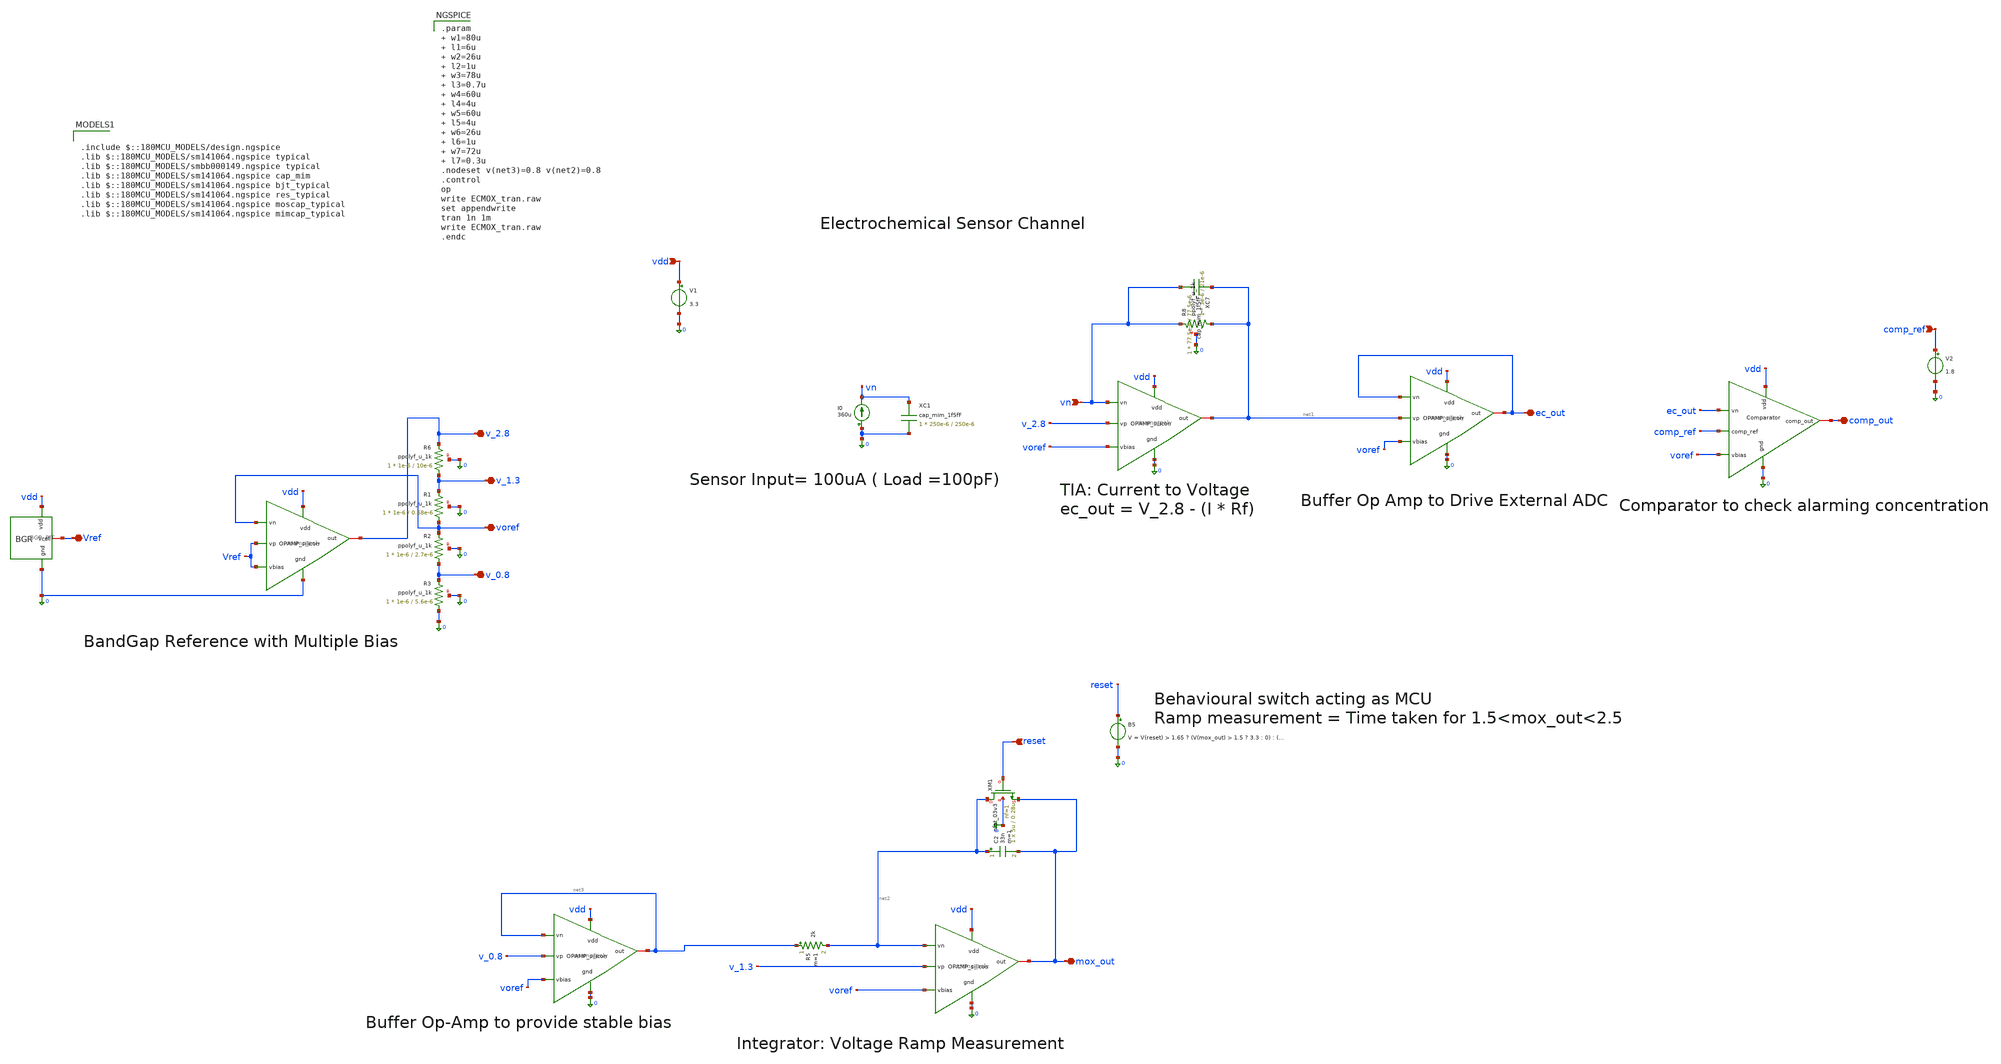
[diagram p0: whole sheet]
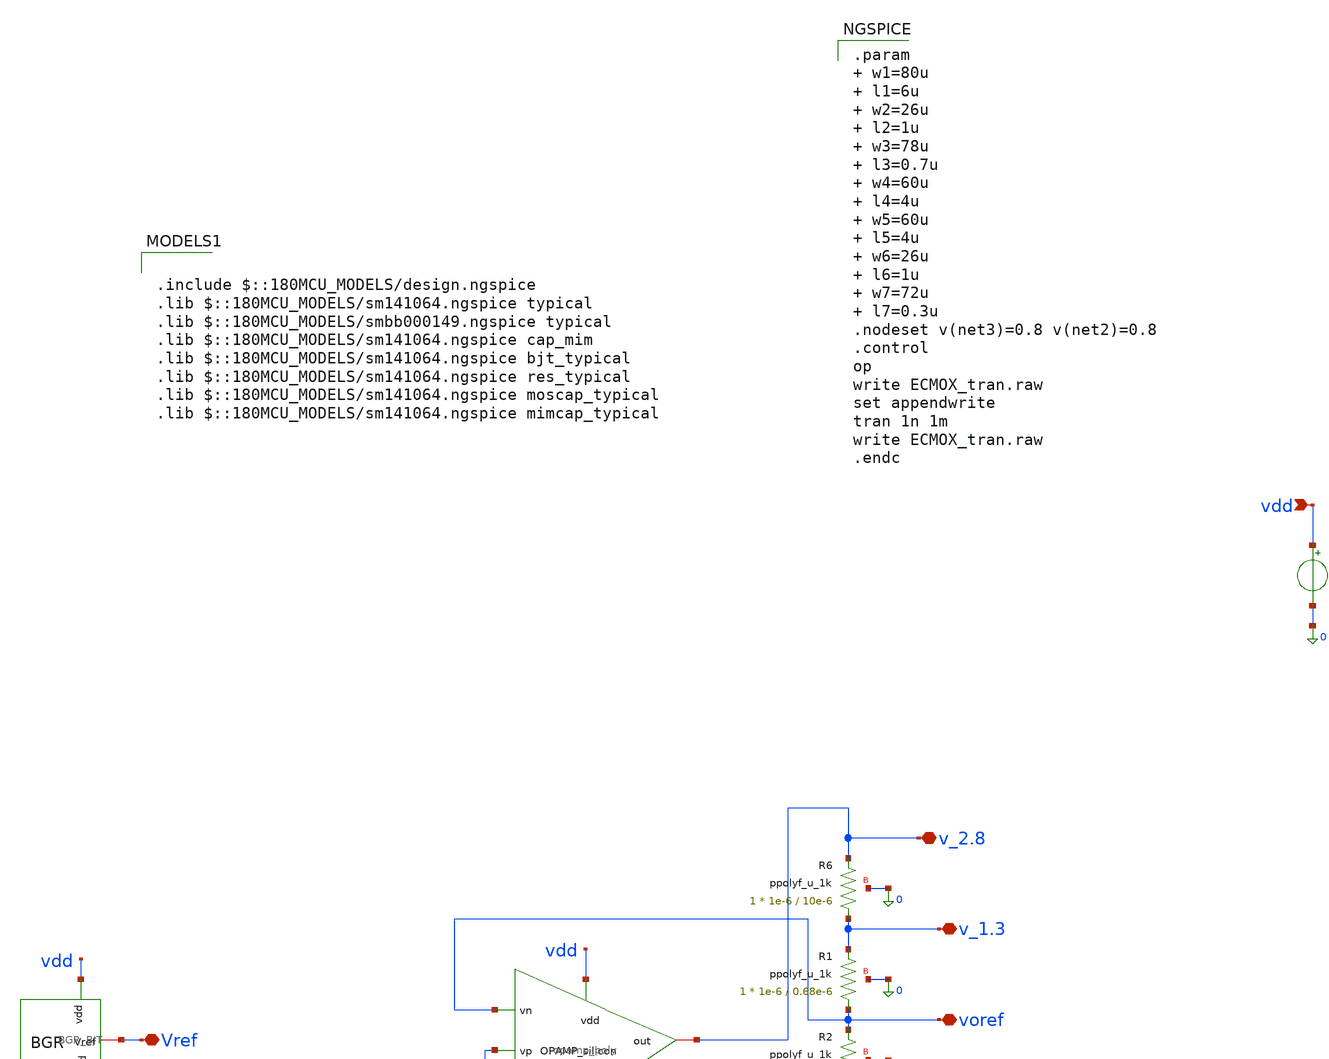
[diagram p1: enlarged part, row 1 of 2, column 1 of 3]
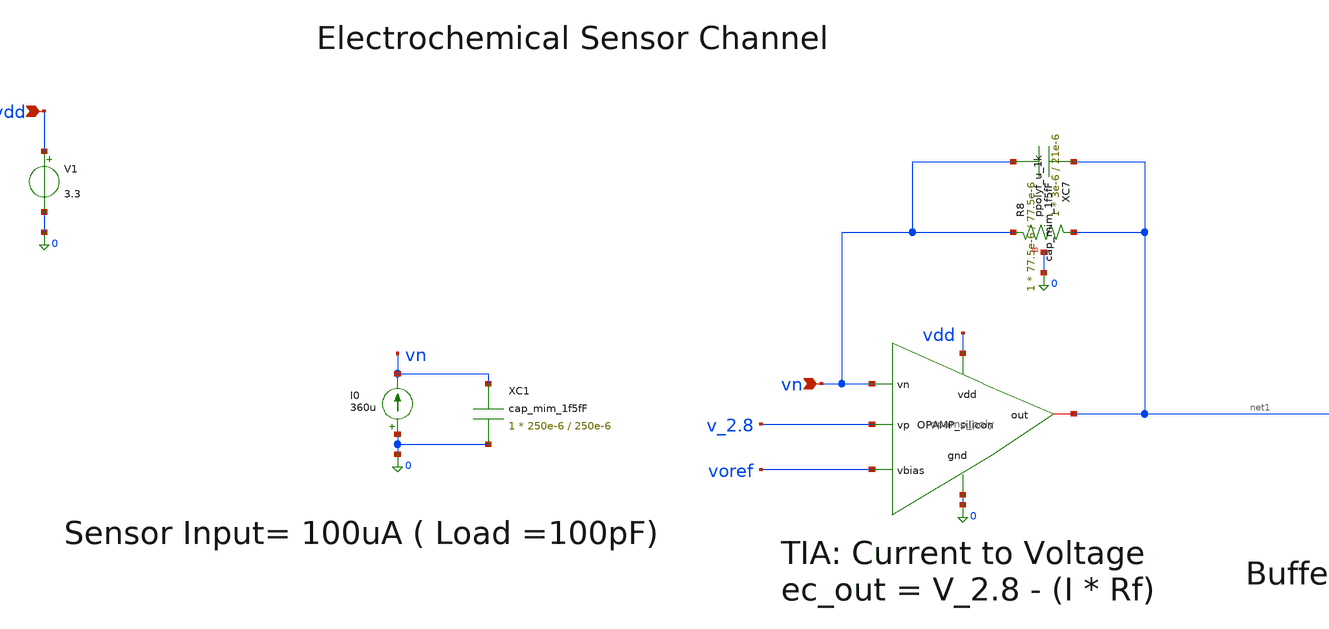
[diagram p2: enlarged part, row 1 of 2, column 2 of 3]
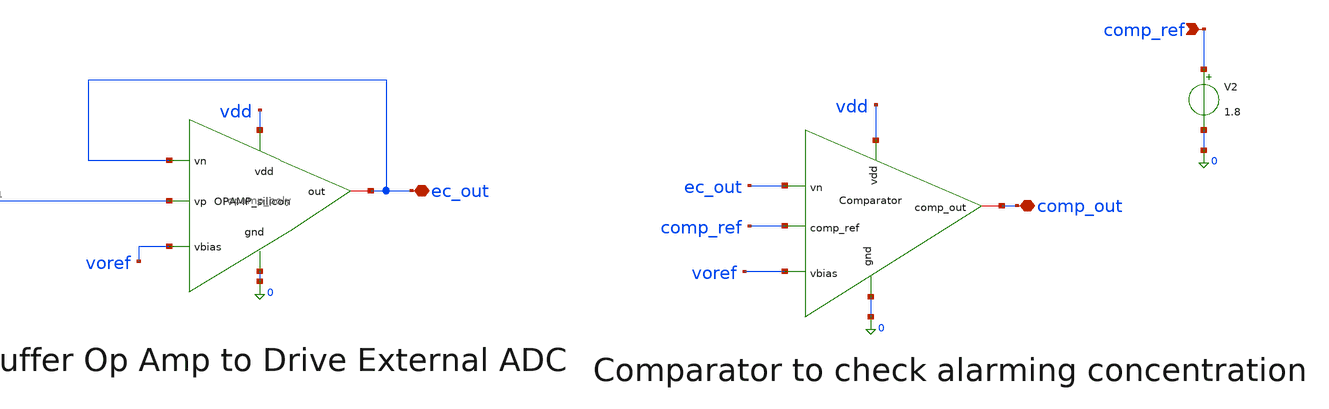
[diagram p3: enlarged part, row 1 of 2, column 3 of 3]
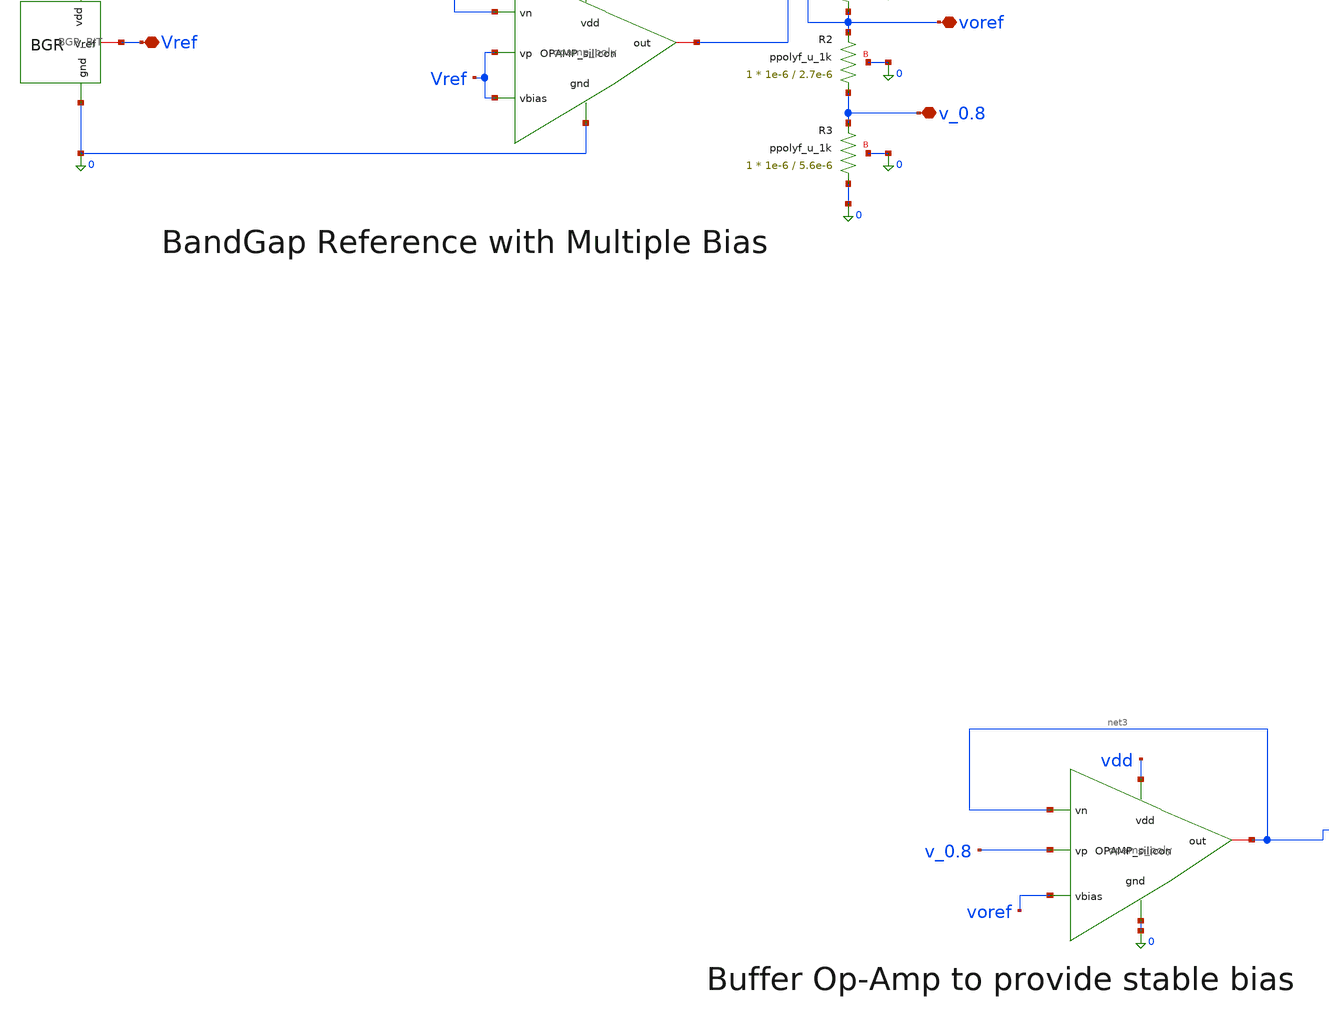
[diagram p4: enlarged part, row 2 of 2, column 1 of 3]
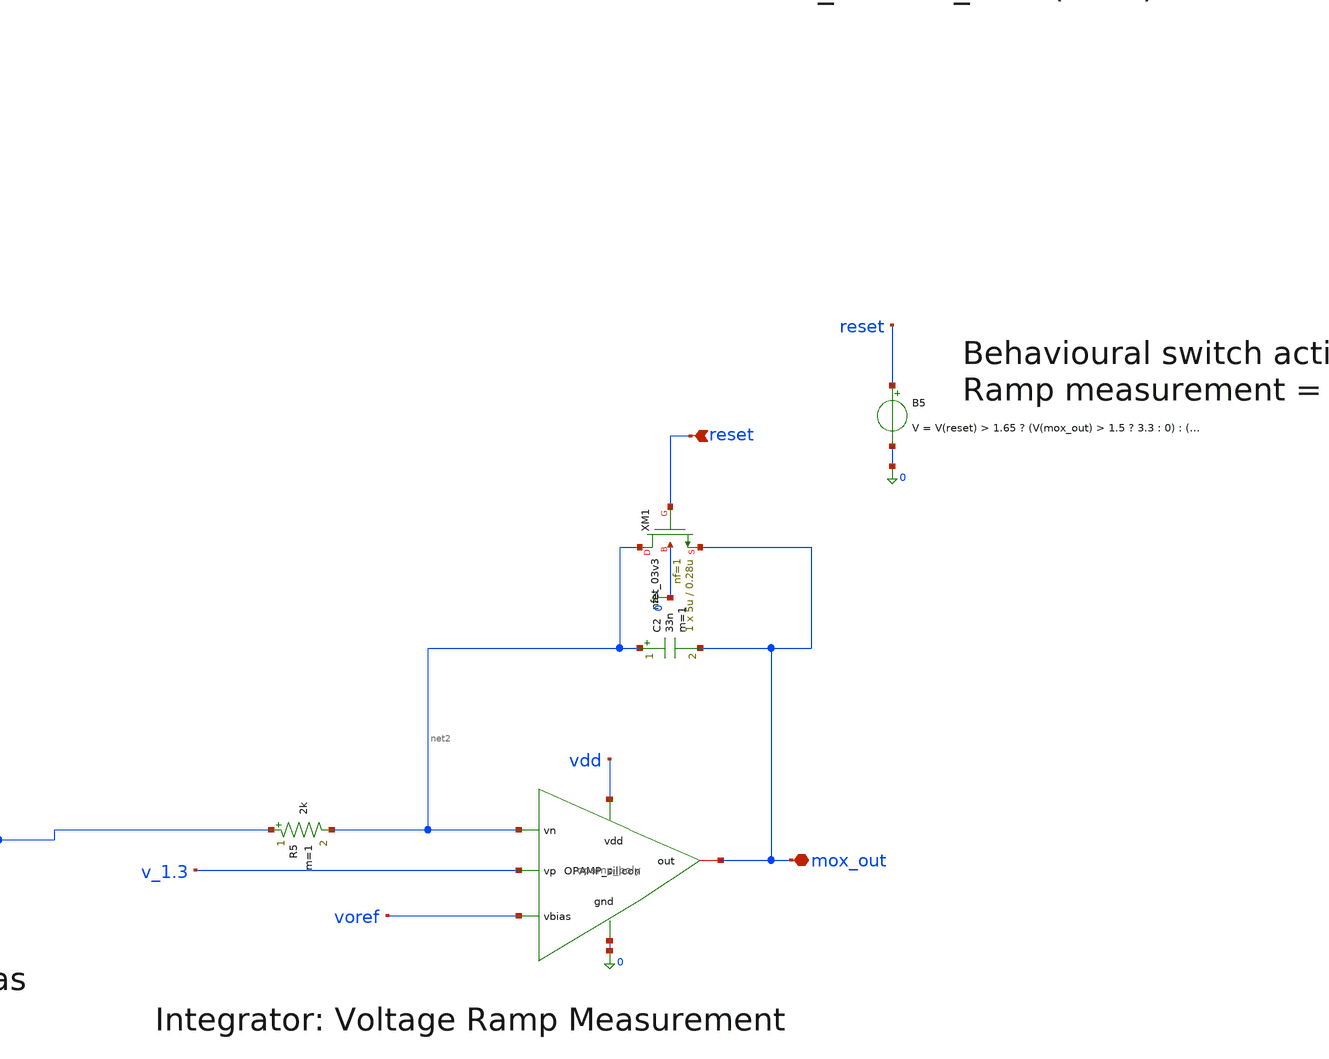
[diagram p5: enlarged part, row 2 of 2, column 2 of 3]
** sch_path: xschem/afe_top/ECMOX_tran.sch
**.subckt ECMOX_tran ec_out vn Vref v_1.3 voref v_0.8 v_2.8 mox_out reset vdd comp_ref comp_out
*.iopin ec_out
*.ipin vn
*.iopin Vref
*.iopin v_1.3
*.iopin voref
*.iopin v_0.8
*.iopin v_2.8
*.iopin mox_out
*.ipin reset
*.ipin vdd
*.ipin comp_ref
*.iopin comp_out
V1 vdd 0 3.3
x2 vdd vn 0 net1 v_2.8 voref opamp_poly
XR8 net1 vn 0 ppolyf_u_1k r_width=3e-6 r_length=21e-6 m=1
XC7 net1 vn cap_mim_1f5fF c_width=77.5e-6 c_length=77.5e-6 m=1
I0 0 vn 360u
XC1 vn 0 cap_mim_1f5fF c_width=250e-6 c_length=250e-6 m=1
x1 vdd voref 0 v_2.8 Vref Vref opamp_poly
x3 vdd Vref 0 BGR_BJT
B5 reset 0 V = V(reset) > 1.65 ? (V(mox_out) > 1.5 ? 3.3 : 0) : (V(mox_out) > 2.5 ? 3.3 : 0)
C2 net2 mox_out 33n m=1
XM1 net2 reset mox_out 0 nfet_03v3 L=0.28u W=5u nf=1 ad='int((nf+1)/2) * W/nf * 0.18u' as='int((nf+2)/2) * W/nf * 0.18u'
+ pd='2*int((nf+1)/2) * (W/nf + 0.18u)' ps='2*int((nf+2)/2) * (W/nf + 0.18u)' nrd='0.18u / W' nrs='0.18u / W'
+ sa=0 sb=0 sd=0 m=1
x4 vdd net2 0 mox_out v_1.3 voref opamp_poly
R5 net3 net2 2k m=1
x5 vdd net3 0 net3 v_0.8 voref opamp_poly
x6 vdd ec_out 0 ec_out net1 voref opamp_poly
XR6 v_1.3 v_2.8 0 ppolyf_u_1k r_width=1e-6 r_length=10e-6 m=1
XR1 voref v_1.3 0 ppolyf_u_1k r_width=1e-6 r_length=0.68e-6 m=1
XR2 v_0.8 voref 0 ppolyf_u_1k r_width=1e-6 r_length=2.7e-6 m=1
XR3 0 v_0.8 0 ppolyf_u_1k r_width=1e-6 r_length=5.6e-6 m=1
x7 vdd ec_out comp_ref voref 0 comp_out comp
V2 comp_ref 0 1.8
**** begin user architecture code

.param  w1=80u       l1=6u  w2=26u       l2=1u  w3=78u     l3=0.7u  w4=60u       l4=4u  w5=60u
+      l5=4u  w6=26u       l6=1u  w7=72u    l7=0.3u
.nodeset v(net3)=0.8 v(net2)=0.8
.control
op
write ECMOX_tran.raw
set appendwrite
tran 1n 1m
write ECMOX_tran.raw
.endc



.include $::180MCU_MODELS/design.ngspice
.lib $::180MCU_MODELS/sm141064.ngspice typical
.lib $::180MCU_MODELS/smbb000149.ngspice typical
.lib $::180MCU_MODELS/sm141064.ngspice cap_mim
.lib $::180MCU_MODELS/sm141064.ngspice bjt_typical
.lib $::180MCU_MODELS/sm141064.ngspice res_typical
.lib $::180MCU_MODELS/sm141064.ngspice moscap_typical
.lib $::180MCU_MODELS/sm141064.ngspice mimcap_typical

**** end user architecture code
**.ends

* expanding   symbol:  GF180/xschem/Chipathon/OpAMP_Silicon/opamp_poly.sym # of pins=6
** sym_path: OpAmP/opamp_poly.sym
** sch_path: OpAmP/opamp_poly.sch
.subckt opamp_poly vdd vn gnd out vp vbias
*.ipin gnd
*.iopin out
*.ipin vbias
*.ipin vp
*.ipin vn
*.ipin vdd
XM1 net3 vbias gnd gnd nfet_03v3 L=l1 W=w1 nf=1 ad='int((nf+1)/2) * W/nf * 0.18u' as='int((nf+2)/2) * W/nf * 0.18u'
+ pd='2*int((nf+1)/2) * (W/nf + 0.18u)' ps='2*int((nf+2)/2) * (W/nf + 0.18u)' nrd='0.18u / W' nrs='0.18u / W'
+ sa=0 sb=0 sd=0 m=1
XM2 net2 net2 vdd vdd pfet_03v3 L=l2 W=w2 nf=1 ad='int((nf+1)/2) * W/nf * 0.18u' as='int((nf+2)/2) * W/nf * 0.18u'
+ pd='2*int((nf+1)/2) * (W/nf + 0.18u)' ps='2*int((nf+2)/2) * (W/nf + 0.18u)' nrd='0.18u / W' nrs='0.18u / W'
+ sa=0 sb=0 sd=0 m=1
XM3 out vbias gnd gnd nfet_03v3 L=l3 W=w3 nf=1 ad='int((nf+1)/2) * W/nf * 0.18u' as='int((nf+2)/2) * W/nf * 0.18u'
+ pd='2*int((nf+1)/2) * (W/nf + 0.18u)' ps='2*int((nf+2)/2) * (W/nf + 0.18u)' nrd='0.18u / W' nrs='0.18u / W'
+ sa=0 sb=0 sd=0 m=1
XM4 net2 vn net3 gnd nfet_03v3 L=l4 W=w4 nf=1 ad='int((nf+1)/2) * W/nf * 0.18u' as='int((nf+2)/2) * W/nf * 0.18u'
+ pd='2*int((nf+1)/2) * (W/nf + 0.18u)' ps='2*int((nf+2)/2) * (W/nf + 0.18u)' nrd='0.18u / W' nrs='0.18u / W'
+ sa=0 sb=0 sd=0 m=1
XM5 net1 vp net3 gnd nfet_03v3 L=l5 W=w5 nf=1 ad='int((nf+1)/2) * W/nf * 0.18u' as='int((nf+2)/2) * W/nf * 0.18u'
+ pd='2*int((nf+1)/2) * (W/nf + 0.18u)' ps='2*int((nf+2)/2) * (W/nf + 0.18u)' nrd='0.18u / W' nrs='0.18u / W'
+ sa=0 sb=0 sd=0 m=1
XM6 net1 net2 vdd vdd pfet_03v3 L=l6 W=w6 nf=1 ad='int((nf+1)/2) * W/nf * 0.18u' as='int((nf+2)/2) * W/nf * 0.18u'
+ pd='2*int((nf+1)/2) * (W/nf + 0.18u)' ps='2*int((nf+2)/2) * (W/nf + 0.18u)' nrd='0.18u / W' nrs='0.18u / W'
+ sa=0 sb=0 sd=0 m=1
XM7 out net1 vdd vdd pfet_03v3 L=l7 W=w7 nf=1 ad='int((nf+1)/2) * W/nf * 0.18u' as='int((nf+2)/2) * W/nf * 0.18u'
+ pd='2*int((nf+1)/2) * (W/nf + 0.18u)' ps='2*int((nf+2)/2) * (W/nf + 0.18u)' nrd='0.18u / W' nrs='0.18u / W'
+ sa=0 sb=0 sd=0 m=1
XR1 net4 net1 gnd ppolyf_u_1k r_width=3e-6 r_length=6.6e-6 m=1
XC1 out net4 cap_mim_1f5fF c_width=20e-6 c_length=20e-6 m=1
.ends


* expanding   symbol:  GF180/xschem/Chipathon/BGR/BGR_BJT.sym # of pins=3
** sym_path: xschem/bias_generator/BGR_BJT.sym
** sch_path: xschem/bias_generator/BGR_BJT.sch
.subckt BGR_BJT vdd Vref gnd
*.ipin gnd
*.iopin Vref
*.ipin vdd
XM2 net1 net2 vdd vdd pfet_03v3 L=4u W=10u nf=1 ad='int((nf+1)/2) * W/nf * 0.18u' as='int((nf+2)/2) * W/nf * 0.18u'
+ pd='2*int((nf+1)/2) * (W/nf + 0.18u)' ps='2*int((nf+2)/2) * (W/nf + 0.18u)' nrd='0.18u / W' nrs='0.18u / W'
+ sa=0 sb=0 sd=0 m=1
XM3 net2 net2 vdd vdd pfet_03v3 L=4u W=10u nf=1 ad='int((nf+1)/2) * W/nf * 0.18u' as='int((nf+2)/2) * W/nf * 0.18u'
+ pd='2*int((nf+1)/2) * (W/nf + 0.18u)' ps='2*int((nf+2)/2) * (W/nf + 0.18u)' nrd='0.18u / W' nrs='0.18u / W'
+ sa=0 sb=0 sd=0 m=1
XM4 Vref net2 vdd vdd pfet_03v3 L=4u W=10u nf=1 ad='int((nf+1)/2) * W/nf * 0.18u' as='int((nf+2)/2) * W/nf * 0.18u'
+ pd='2*int((nf+1)/2) * (W/nf + 0.18u)' ps='2*int((nf+2)/2) * (W/nf + 0.18u)' nrd='0.18u / W' nrs='0.18u / W'
+ sa=0 sb=0 sd=0 m=1
XM13 net1 net1 net5 gnd nfet_03v3 L=2u W=10u nf=1 ad='int((nf+1)/2) * W/nf * 0.18u' as='int((nf+2)/2) * W/nf * 0.18u'
+ pd='2*int((nf+1)/2) * (W/nf + 0.18u)' ps='2*int((nf+2)/2) * (W/nf + 0.18u)' nrd='0.18u / W' nrs='0.18u / W'
+ sa=0 sb=0 sd=0 m=1
XM14 net2 net1 net4 gnd nfet_03v3 L=2u W=10u nf=1 ad='int((nf+1)/2) * W/nf * 0.18u' as='int((nf+2)/2) * W/nf * 0.18u'
+ pd='2*int((nf+1)/2) * (W/nf + 0.18u)' ps='2*int((nf+2)/2) * (W/nf + 0.18u)' nrd='0.18u / W' nrs='0.18u / W'
+ sa=0 sb=0 sd=0 m=1
R1 Vref net7 66k m=1
R2 net4 net3 5k m=1
XQ1 gnd gnd net3 pnp_05p00x05p00 m=4 par=4
XQ2 gnd gnd net5 pnp_05p00x05p00 m=1 par=1
XM1 net2 net6 gnd gnd nfet_03v3 L=2u W=10u nf=1 ad='int((nf+1)/2) * W/nf * 0.18u' as='int((nf+2)/2) * W/nf * 0.18u'
+ pd='2*int((nf+1)/2) * (W/nf + 0.18u)' ps='2*int((nf+2)/2) * (W/nf + 0.18u)' nrd='0.18u / W' nrs='0.18u / W'
+ sa=0 sb=0 sd=0 m=1
XM5 vdd vdd net6 gnd nfet_03v3 L=0.5u W=1u nf=1 ad='int((nf+1)/2) * W/nf * 0.18u' as='int((nf+2)/2) * W/nf * 0.18u'
+ pd='2*int((nf+1)/2) * (W/nf + 0.18u)' ps='2*int((nf+2)/2) * (W/nf + 0.18u)' nrd='0.18u / W' nrs='0.18u / W'
+ sa=0 sb=0 sd=0 m=1
XM6 net6 net1 gnd gnd nfet_03v3 L=1u W=20u nf=1 ad='int((nf+1)/2) * W/nf * 0.18u' as='int((nf+2)/2) * W/nf * 0.18u'
+ pd='2*int((nf+1)/2) * (W/nf + 0.18u)' ps='2*int((nf+2)/2) * (W/nf + 0.18u)' nrd='0.18u / W' nrs='0.18u / W'
+ sa=0 sb=0 sd=0 m=1
XQ3 gnd gnd net7 pnp_05p00x05p00 m=1 par=1
.ends


* expanding   symbol:  GF180/xschem/Chipathon/Comparator/comp.sym # of pins=6
** sym_path: xschem/comparator/comp.sym
** sch_path: xschem/comparator/comp.sch
.subckt comp vdd vn comp_ref vbias gnd comp_out
*.ipin vn
*.ipin vbias
*.ipin vdd
*.ipin comp_ref
*.iopin comp_out
*.ipin gnd
XM1 net2 net1 gnd gnd nfet_03v3 L=0.28u W=0.22u nf=1 ad='int((nf+1)/2) * W/nf * 0.18u' as='int((nf+2)/2) * W/nf * 0.18u'
+ pd='2*int((nf+1)/2) * (W/nf + 0.18u)' ps='2*int((nf+2)/2) * (W/nf + 0.18u)' nrd='0.18u / W' nrs='0.18u / W'
+ sa=0 sb=0 sd=0 m=1
XM2 net2 net1 vdd vdd pfet_03v3 L=0.28u W=0.22u nf=1 ad='int((nf+1)/2) * W/nf * 0.18u' as='int((nf+2)/2) * W/nf * 0.18u'
+ pd='2*int((nf+1)/2) * (W/nf + 0.18u)' ps='2*int((nf+2)/2) * (W/nf + 0.18u)' nrd='0.18u / W' nrs='0.18u / W'
+ sa=0 sb=0 sd=0 m=1
XM5 comp_out net2 gnd gnd nfet_03v3 L=0.28u W=0.22u nf=1 ad='int((nf+1)/2) * W/nf * 0.18u' as='int((nf+2)/2) * W/nf * 0.18u'
+ pd='2*int((nf+1)/2) * (W/nf + 0.18u)' ps='2*int((nf+2)/2) * (W/nf + 0.18u)' nrd='0.18u / W' nrs='0.18u / W'
+ sa=0 sb=0 sd=0 m=1
XM6 comp_out net2 vdd vdd pfet_03v3 L=0.28u W=0.22u nf=1 ad='int((nf+1)/2) * W/nf * 0.18u' as='int((nf+2)/2) * W/nf * 0.18u'
+ pd='2*int((nf+1)/2) * (W/nf + 0.18u)' ps='2*int((nf+2)/2) * (W/nf + 0.18u)' nrd='0.18u / W' nrs='0.18u / W'
+ sa=0 sb=0 sd=0 m=1
x1 vdd vn gnd net1 net3 vbias opamp_poly
XR3 net3 comp_ref gnd ppolyf_u_1k r_width=1e-6 r_length=20e-6 m=1
XR1 net1 net3 gnd ppolyf_u_1k r_width=1e-6 r_length=500e-6 m=1
.ends

.end
